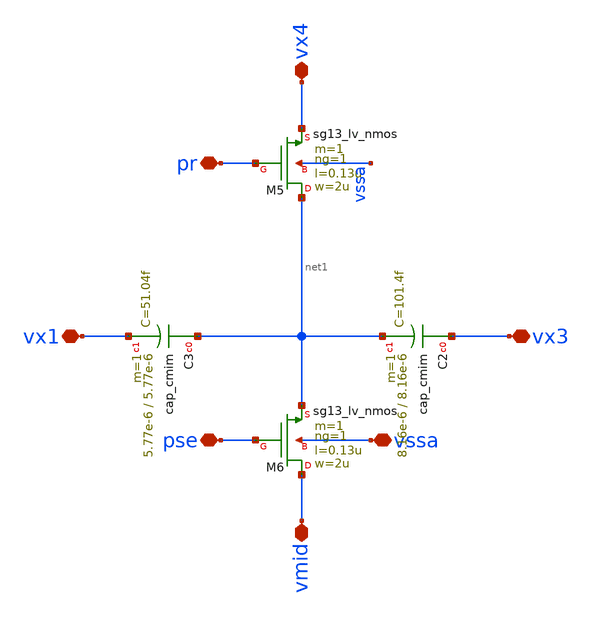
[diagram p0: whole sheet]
** sch_path: 5_Design/4_Layout/Team 5/splitUpSimulationsAndSchematics/integ_5_split4.sch
**.subckt integ_5_split4 vssa vx1 pse vmid vx3 pr vx4
*.iopin vssa
*.iopin vx1
*.iopin pse
*.iopin vmid
*.iopin vx3
*.iopin pr
*.iopin vx4
XC2 vx3 net1 cap_cmim w=8.16e-6 l=8.16e-6 m=1 mm_ok=1
XM5 net1 pr vx4 vssa sg13_lv_nmos w=2u l=0.13u ng=1 m=1 mm_ok=1
XM6 vmid pse net1 vssa sg13_lv_nmos w=2u l=0.13u ng=1 m=1 mm_ok=1
XC3 net1 vx1 cap_cmim w=5.77e-6 l=5.77e-6 m=1 mm_ok=1
**.ends
.end
